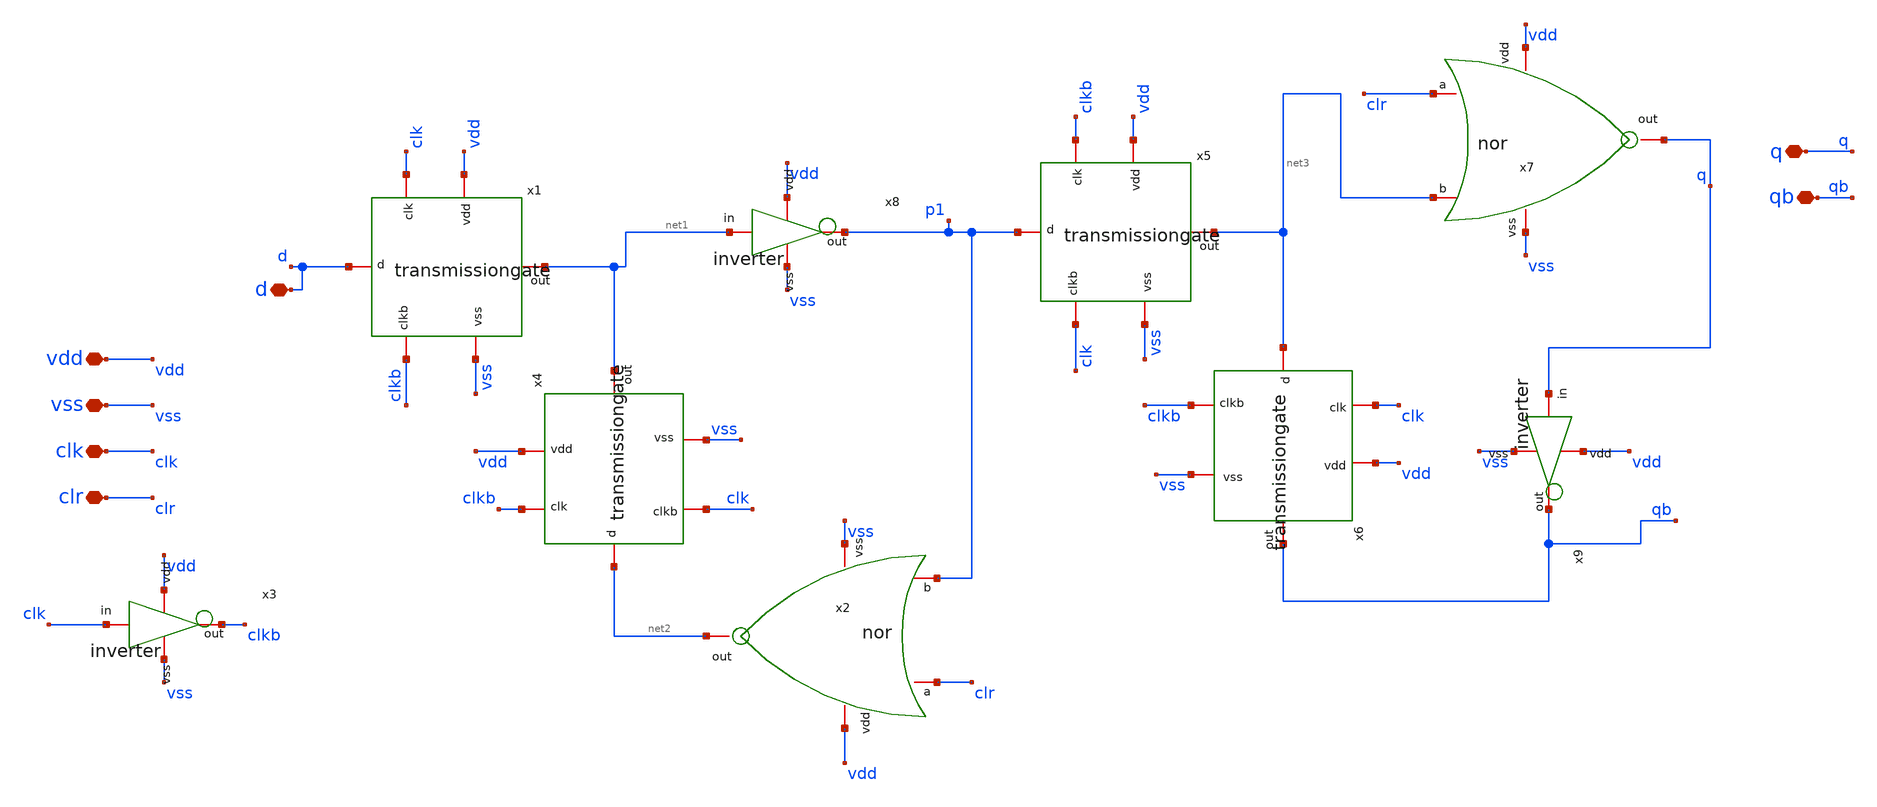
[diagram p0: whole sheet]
** sch_path: design/blocks/dff/schematic/dff.sch
**.subckt dff d clk clr q qb vdd vss
*.iopin d
*.iopin clk
*.iopin clr
*.iopin q
*.iopin qb
*.iopin vdd
*.iopin vss
x1 clk vss net1 d vdd clkb transmissiongate
x2 vdd clr p1 net2 vss nor
x3 vdd clkb clk vss inverter
x4 clkb vss net1 net2 vdd clk transmissiongate
x5 clkb vss net3 p1 vdd clk transmissiongate
x6 clk vss qb net3 vdd clkb transmissiongate
x7 vdd clr net3 q vss nor
x8 vdd p1 net1 vss inverter
x9 vdd qb q vss inverter
**.ends

* expanding   symbol:  blocks/transmissiongate/schematic/transmissiongate.sym # of pins=6
** sym_path: design/blocks/transmissiongate/schematic/transmissiongate.sym
** sch_path: design/blocks/transmissiongate/schematic/transmissiongate.sch
.subckt transmissiongate clk vss out d vdd clkb
*.iopin out
*.iopin d
*.iopin clkb
*.iopin clk
*.iopin vdd
*.iopin vss
XM1 out clkb d vdd sg13_lv_pmos w=1.5u l=0.15u ng=1 m=1 mm_ok=1
XM0 d clk out vss sg13_lv_nmos w=0.75u l=0.15u ng=1 m=1 mm_ok=1
.ends


* expanding   symbol:  blocks/norgate/schematic/nor.sym # of pins=5
** sym_path: design/blocks/norgate/schematic/nor.sym
** sch_path: design/blocks/norgate/schematic/nor.sch
.subckt nor vdd a b out vss
*.iopin vdd
*.iopin a
*.iopin vss
*.iopin out
*.iopin b
XM1 net1 a vdd vdd sg13_lv_pmos w=3.0u l=0.15u ng=1 m=1 mm_ok=1
XM2 out b vss vss sg13_lv_nmos w=0.75u l=0.15u ng=1 m=1 mm_ok=1
XM3 out a vss vss sg13_lv_nmos w=0.75u l=0.15u ng=1 m=1 mm_ok=1
XM4 out b net1 vdd sg13_lv_pmos w=3.0u l=0.15u ng=1 m=1 mm_ok=1
.ends


* expanding   symbol:  blocks/inverter/schematic/inverter.sym # of pins=4
** sym_path: design/blocks/inverter/schematic/inverter.sym
** sch_path: design/blocks/inverter/schematic/inverter.sch
.subckt inverter vdd out in vss
*.iopin vdd
*.iopin out
*.iopin vss
*.iopin in
XM1 out in vss vss sg13_lv_nmos w=0.75u l=0.15u ng=1 m=1 mm_ok=1
XM2 out in vdd vdd sg13_lv_pmos w=1.5u l=0.15u ng=1 m=1 mm_ok=1
.ends

.end
